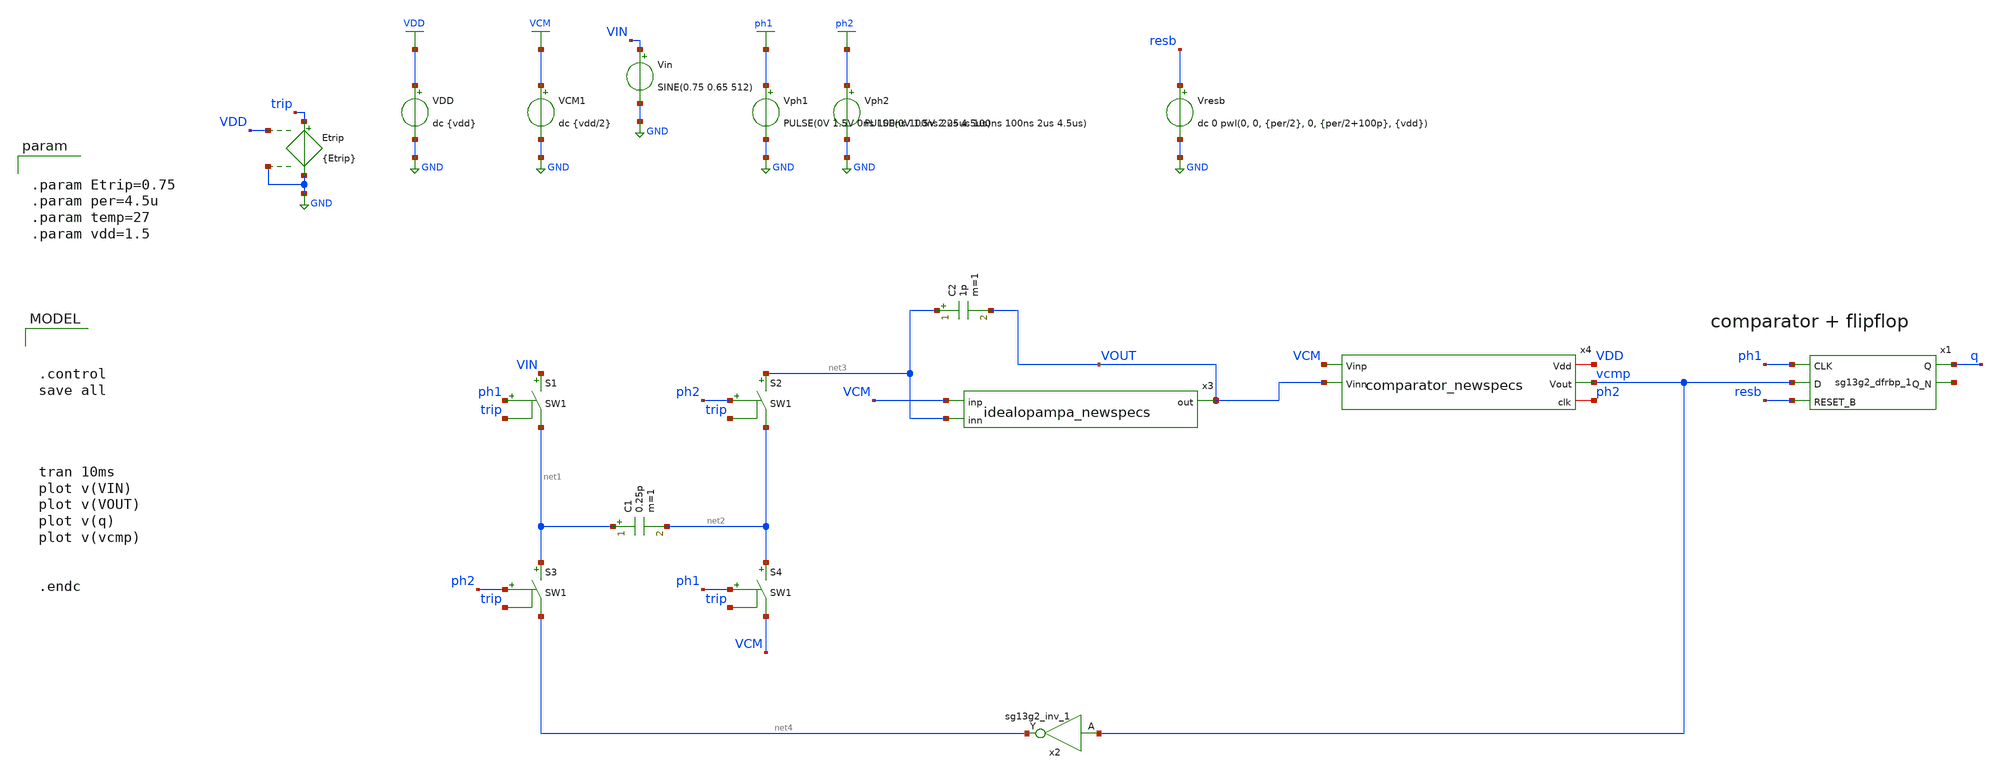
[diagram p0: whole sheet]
** sch_path: DSM_1storder/Schematic_Level/xschem/DSM_1storder_newspecs.sch
**.subckt DSM_1storder_newspecs
C1 net1 net2 0.25p m=1
S2 net3 net2 ph2 trip SW1
S3 net1 net4 ph2 trip SW1
S4 net2 VCM ph1 trip SW1
VDD VDD GND dc {vdd}
VCM1 VCM GND dc {vdd/2}
Vph2 ph2 GND PULSE(0V 1.5V 2.25us 100ns 100ns 2us 4.5us)
Vph1 ph1 GND PULSE(0V 1.5V 0ns 100ns 100ns 2us 4.5us)
C2 net3 VOUT 1p m=1
x1 q net5 ph1 vcmp resb VDD VSS sg13g2_dfrbp_1
Vresb resb GND dc 0 pwl(0, 0, {per/2}, 0, {per/2+100p}, {vdd})
x2 net4 vcmp VDD VSS sg13g2_inv_1
S1 VIN net1 ph1 trip SW1
Etrip trip GND VDD GND {Etrip}
Vin VIN GND SINE(0.75 0.65 512)
x3 VOUT VCM net3 idealopampa_newspecs
x4 VDD vcmp VCM ph2 VOUT comparator_newspecs
**** begin user architecture code



.control
save all




tran 10ms
plot v(VIN)
plot v(VOUT)
plot v(q)
plot v(vcmp)


.endc



.lib $::SG13G2_MODELS/cornerMOSlv.lib mos_tt
.lib $::SG13G2_MODELS/cornerRES.lib res_typ
.inc /foss/pdks/ihp-sg13g2/libs.ref/sg13g2_stdcell/spice/sg13g2_stdcell.spice



.param Etrip=0.75
.param per=4.5u
.param temp=27
.param vdd=1.5


**** end user architecture code
**.ends

* expanding   symbol:  sg13g2_stdcells/sg13g2_dfrbp_1.sym # of pins=5
** sym_path: sg13g2_stdcells/sg13g2_dfrbp_1.sym
** sch_path: sg13g2_stdcells/sg13g2_dfrbp_1.sch
.subckt sg13g2_dfrbp_1 Q Q_N CLK D RESET_B VDD VSS
*.ipin D
*.ipin RESET_B
*.ipin CLK
*.opin Q
*.opin Q_N
*.iopin VDD
*.iopin VSS
XM1 Db D net10 VSS sg13_lv_nmos w=420.00n l=130.00n ng=1 m=1 mm_ok=1
XM2 net10 RESET_B VSS VSS sg13_lv_nmos w=420.00n l=130.00n ng=1 m=1 mm_ok=1
XM3 net1 clkneg net9 VSS sg13_lv_nmos w=420.00n l=130.00n ng=1 m=1 mm_ok=1
XM4 net9 net1 VSS VSS sg13_lv_nmos w=420.00n l=130.00n ng=1 m=1 mm_ok=1
XM5 net1 net1 net5 VSS sg13_lv_nmos w=420.00n l=130.00n ng=1 m=1 mm_ok=1
XM6 net5 RESET_B VSS VSS sg13_lv_nmos w=420.00n l=130.00n ng=1 m=1 mm_ok=1
XM7 Q_N net1 VSS VSS sg13_lv_nmos w=740.00n l=130.00n ng=1 m=1 mm_ok=1
XM8 net2 net1 VSS VSS sg13_lv_nmos w=740.00n l=130.00n ng=1 m=1 mm_ok=1
XM9 Q net2 VSS VSS sg13_lv_nmos w=740.00n l=130.00n ng=1 m=1 mm_ok=1
XM10 clkneg CLK VSS VSS sg13_lv_nmos w=740.00n l=130.00n ng=1 m=1 mm_ok=1
XM11 clkpos clkneg VSS VSS sg13_lv_nmos w=740.00n l=130.00n ng=1 m=1 mm_ok=1
XM12 Db clkneg net3 VSS sg13_lv_nmos w=420.00n l=130.00n ng=1 m=1 mm_ok=1
XM13 net3 clkpos net8 VSS sg13_lv_nmos w=420.00n l=130.00n ng=1 m=1 mm_ok=1
XM14 net8 net3 net4 VSS sg13_lv_nmos w=420.00n l=130.00n ng=1 m=1 mm_ok=1
XM15 net4 RESET_B VSS VSS sg13_lv_nmos w=420.00n l=130.00n ng=1 m=1 mm_ok=1
XM16 net3 net3 VSS VSS sg13_lv_nmos w=740.00n l=130.00n ng=1 m=1 mm_ok=1
XM17 net3 clkpos net1 VSS sg13_lv_nmos w=740.00n l=130.00n ng=1 m=1 mm_ok=1
XM18 Db RESET_B VDD VDD sg13_lv_pmos w=420.00n l=130.00n ng=1 m=1 mm_ok=1
XM19 Db D VDD VDD sg13_lv_pmos w=420.00n l=130.00n ng=1 m=1 mm_ok=1
XM20 net7 net1 VDD VDD sg13_lv_pmos w=420.00n l=130.00n ng=1 m=1 mm_ok=1
XM21 net1 clkpos net7 VDD sg13_lv_pmos w=420.00n l=130.00n ng=1 m=1 mm_ok=1
XM22 net1 net1 VDD VDD sg13_lv_pmos w=420.00n l=130.00n ng=1 m=1 mm_ok=1
XM23 net1 RESET_B VDD VDD sg13_lv_pmos w=420.00n l=130.00n ng=1 m=1 mm_ok=1
XM24 Q_N net1 VDD VDD sg13_lv_pmos w=1.12u l=130.00n ng=1 m=1 mm_ok=1
XM25 net2 net1 VDD VDD sg13_lv_pmos w=1.12u l=130.00n ng=1 m=1 mm_ok=1
XM26 Q net2 VDD VDD sg13_lv_pmos w=1.12u l=130.00n ng=1 m=1 mm_ok=1
XM27 clkneg CLK VDD VDD sg13_lv_pmos w=1.12u l=130.00n ng=1 m=1 mm_ok=1
XM28 clkpos clkneg VDD VDD sg13_lv_pmos w=1.12u l=130.00n ng=1 m=1 mm_ok=1
XM29 Db clkpos net3 VDD sg13_lv_pmos w=420.00n l=130.00n ng=1 m=1 mm_ok=1
XM30 net6 net3 VDD VDD sg13_lv_pmos w=420.00n l=130.00n ng=1 m=1 mm_ok=1
XM31 net3 clkneg net6 VDD sg13_lv_pmos w=420.00n l=130.00n ng=1 m=1 mm_ok=1
XM32 net3 RESET_B VDD VDD sg13_lv_pmos w=420.00n l=130.00n ng=1 m=1 mm_ok=1
XM33 net3 net3 VDD VDD sg13_lv_pmos w=1.000u l=130.00n ng=1 m=1 mm_ok=1
XM34 net3 clkneg net1 VDD sg13_lv_pmos w=1.000u l=130.00n ng=1 m=1 mm_ok=1
.ends


* expanding   symbol:  sg13g2_stdcells/sg13g2_inv_1.sym # of pins=2
** sym_path: sg13g2_stdcells/sg13g2_inv_1.sym
** sch_path: sg13g2_stdcells/sg13g2_inv_1.sch
.subckt sg13g2_inv_1 Y A VDD VSS
*.opin Y
*.ipin A
*.iopin VDD
*.iopin VSS
XM1 Y A VSS VSS sg13_lv_nmos w=740.00n l=130.00n ng=1 m=1 mm_ok=1
XM2 Y A VDD VDD sg13_lv_pmos w=1.12u l=130.00n ng=1 m=1 mm_ok=1
.ends


* expanding   symbol:  idealopampa_newspecs.sym # of pins=3
** sym_path: DSM_1storder/Schematic_Level/xschem/idealopampa_newspecs.sym
** sch_path: DSM_1storder/Schematic_Level/xschem/idealopampa_newspecs.sch
.subckt idealopampa_newspecs out inp inn
*.opin out
*.ipin inp
*.ipin inn
E1 net1 GND inp inn 1Meg
R1 out GND 100Meg m=1
R2 net1 out 1000 m=1
.ends


* expanding   symbol:  comparator_newspecs.sym # of pins=5
** sym_path: DSM_1storder/Schematic_Level/xschem/comparator_newspecs.sym
** sch_path: DSM_1storder/Schematic_Level/xschem/comparator_newspecs.sch
.subckt comparator_newspecs Vdd Vout Vinp clk Vinn
*.ipin Vinp
*.ipin Vinn
*.opin Vout
*.iopin Vdd
*.iopin clk
E1 diff GND Vinp Vinn 1
S1 diff sample tp clk SW1
E2 net1 GND sample GND 1
C1 sample GND 100p m=1
S2 net1 hold clk tp SW1
C2 hold GND 100p m=1
B1 net2 GND V={v(hold)>0?v(Vdd):0}
Etp tp GND Vdd GND 0.75
**** begin user architecture code


.ic v(hold)=1 v(sample)=1


**** end user architecture code
**** begin user architecture code

.param vdd=1.5

**** end user architecture code
C3 Vout GND 100f m=1
R2 net2 Vout 1000 m=1
.ends

.GLOBAL GND
.GLOBAL VDD
.GLOBAL VCM
.GLOBAL ph2
.GLOBAL ph1
**** begin user architecture code
.MODEL SW1 SW( VT=0.4 VH=0.01 RON=0.01 ROFF=10G )
**** end user architecture code
.end
